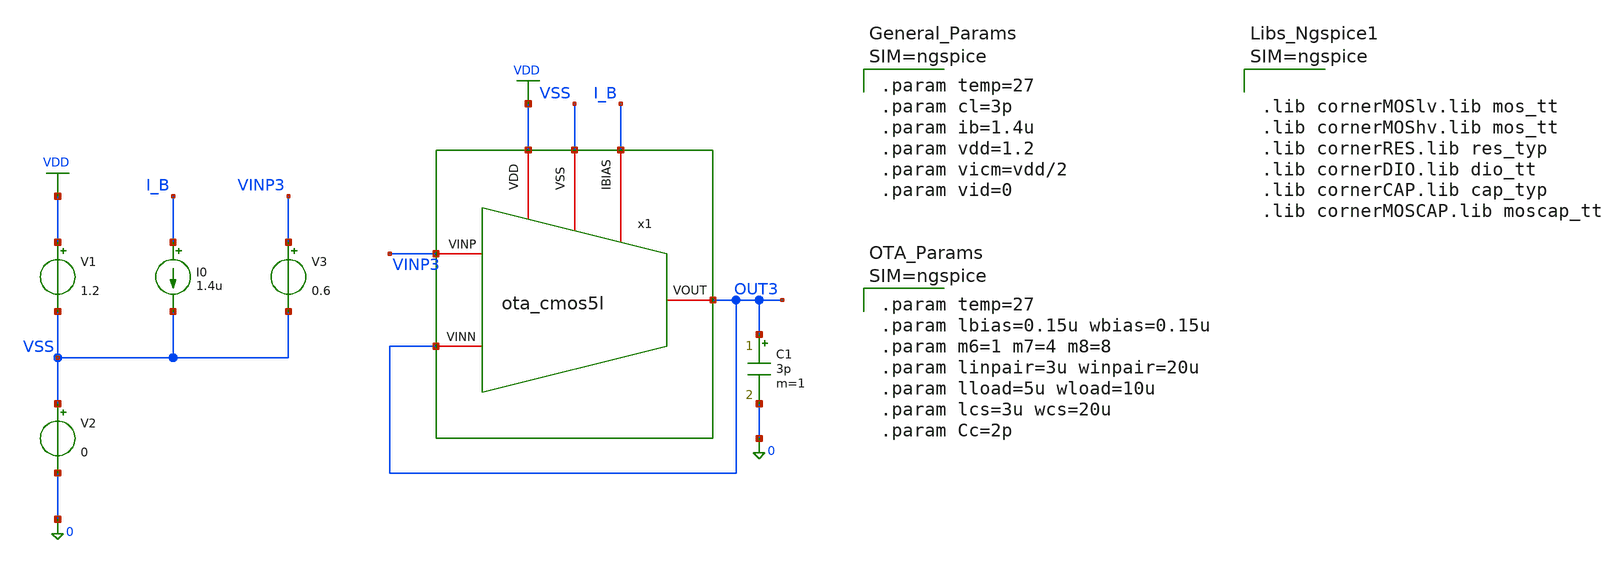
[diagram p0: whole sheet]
** sch_path: xschem/ota_cmos5l/tb/tb_ota_cmos5l_DC_close_loop_op/tb_ota_cmos5l_DC_close_loop_op.sch
**.subckt tb_ota_cmos5l_DC_close_loop_op
x1 VSS I_B VDD OUT3 VINP3 OUT3 ota_cmos5l
C1 OUT3 0 3p m=1
I0 I_B VSS 1.4u
V1 VDD VSS 1.2
V2 VSS 0 0
V3 VINP3 VSS 0.6
**** begin user architecture code



.lib cornerMOSlv.lib mos_tt
.lib cornerMOShv.lib mos_tt
.lib cornerRES.lib res_typ
.lib cornerDIO.lib dio_tt
.lib cornerCAP.lib cap_typ
.lib cornerMOSCAP.lib moscap_tt





.param temp=27
.param cl=3p
.param ib=1.4u
.param vdd=1.2
.param vicm=vdd/2
.param vid=0





.param temp=27
.param lbias=0.15u wbias=0.15u
.param m6=1 m7=4 m8=8
.param linpair=3u winpair=20u
.param lload=5u wload=10u
.param lcs=3u wcs=20u
.param Cc=2p





.op
.control
save all
op
shell mkdir -p result
run
write ./result/tb_cg_ota_dc-close-op.raw
show all : m, l, w, vgs, vds, vth, ids, vsat, gm, gds, fug, ids
let v_in = v(vinp3)
let v_out = v(out3)
let vos_mv = (v_in - v_out) * 1000
let i_q = -i(v1)
let p_q = i_q * 1.2
let p_q_uw = p_q * 1e6
let i_q_ua = i_q * 1e6
echo "======================================================="
echo " Input Common-Mode (Vin+): " $&v_in " V"
echo " Output Voltage (Vout): " $&v_out " V"
echo " Systematic Offset (Vos): " $&vos_mv " mV"
echo " Quiescent Current (I_q): " $&i_q_ua " uA"
echo " Quiescent Power (P_q): " $&p_q_uw " uW"
echo "======================================================="
.endc



**** end user architecture code
**.ends

* expanding   symbol:  /foss/designs/sg13cmos5l_spma_ip__instramp/xschem/ota_cmos5l/ota_cmos5l.sym #
*+ of pins=6
** sym_path: xschem/output_buffer/ota_cmos5l.sym
** sch_path: xschem/output_buffer/ota_cmos5l.sch
.subckt ota_cmos5l VSS IBIAS VDD VINN VINP VOUT
*.iopin IBIAS
*.iopin VDD
*.iopin VSS
*.iopin VOUT
*.iopin VINP
*.iopin VINN
XM6 IBIAS IBIAS VDD VDD sg13_lv_pmos w={wbias} l={lbias} ng=1 m={m6} mm_ok=1
XM7 net1 IBIAS VDD VDD sg13_lv_pmos w={wbias} l={lbias} ng=1 m={m7} mm_ok=1
XM8 VOUT IBIAS VDD VDD sg13_lv_pmos w={wbias} l={lbias} ng=1 m={m8} mm_ok=1
XM1 net2 VINN net1 VDD sg13_lv_pmos w={winpair} l={linpair} ng=1 m=1 mm_ok=1
XM2 net3 VINP net1 VDD sg13_lv_pmos w={winpair} l={linpair} ng=1 m=1 mm_ok=1
XM3 net2 net2 VSS VSS sg13_lv_nmos w={wload} l={lload} ng=1 m=1 mm_ok=1
XM4 net3 net2 VSS VSS sg13_lv_nmos w={wload} l={lload} ng=1 m=1 mm_ok=1
XM5 VOUT net3 VSS VSS sg13_lv_nmos w={wcs} l={lcs} ng=1 m=1 mm_ok=1
XR1 net3 net4 VSS rhigh w=0.5e-6 l=1.95e-6 m=1 b=0 mm_ok=1
.save v(vinp)
.save v(vinn)
.save v(vout)
XC2 VOUT net4 cap_cmomi w=15e-6 l=15e-6 mmin=1 mmax=4 feed=double subblock=0 m=5 mm_ok=1
**** begin user architecture code


.param temp=27
.param lbias=0.15u wbias=0.15u
.param m6=1 m7=4 m8=8
.param linpair=3u winpair=20u
.param lload=5u wload=10u
.param lcs=3u wcs=20u
.param Cc=2p



**** end user architecture code
XC1 VOUT net4 cap_cmomi w=15e-6 l=15e-6 mmin=1 mmax=4 feed=double subblock=0 m=4 mm_ok=1
.ends

.GLOBAL VDD
.end
